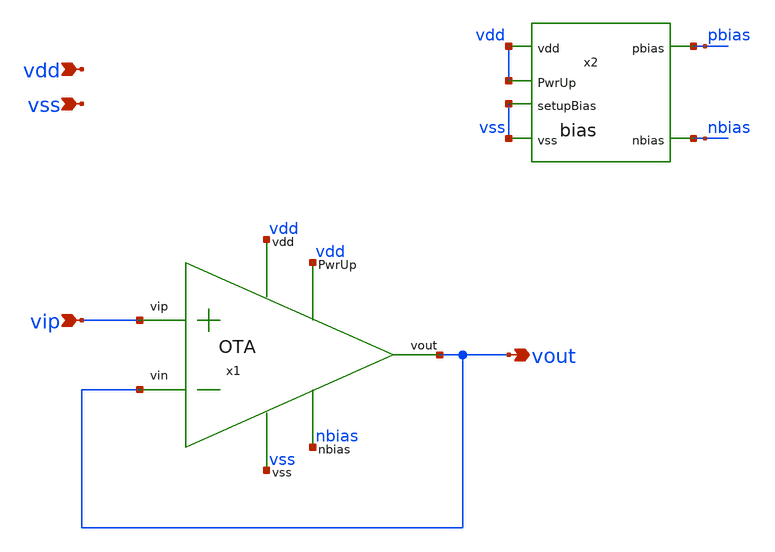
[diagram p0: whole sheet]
** sch_path: design/JNW_AVV_SKY130A/TB_OTA.sch
**.subckt TB_OTA vip vss vdd vout
*.ipin vip
*.ipin vss
*.ipin vdd
*.opin vout
x1 vdd vout vout vip vss nbias vdd OTA
x2 pbias vdd nbias vss vss vdd bias
**.ends
.end
